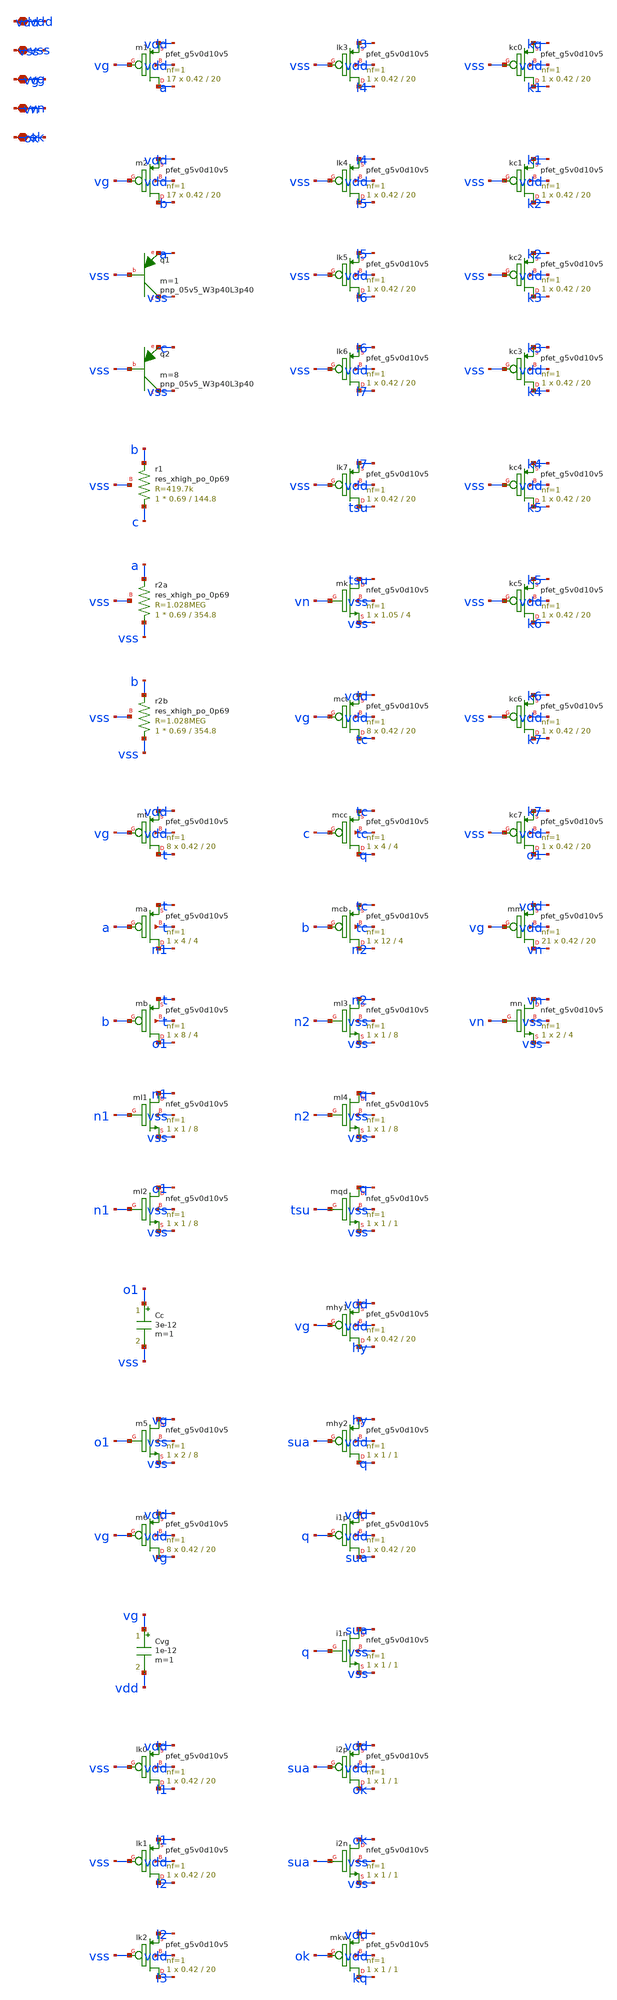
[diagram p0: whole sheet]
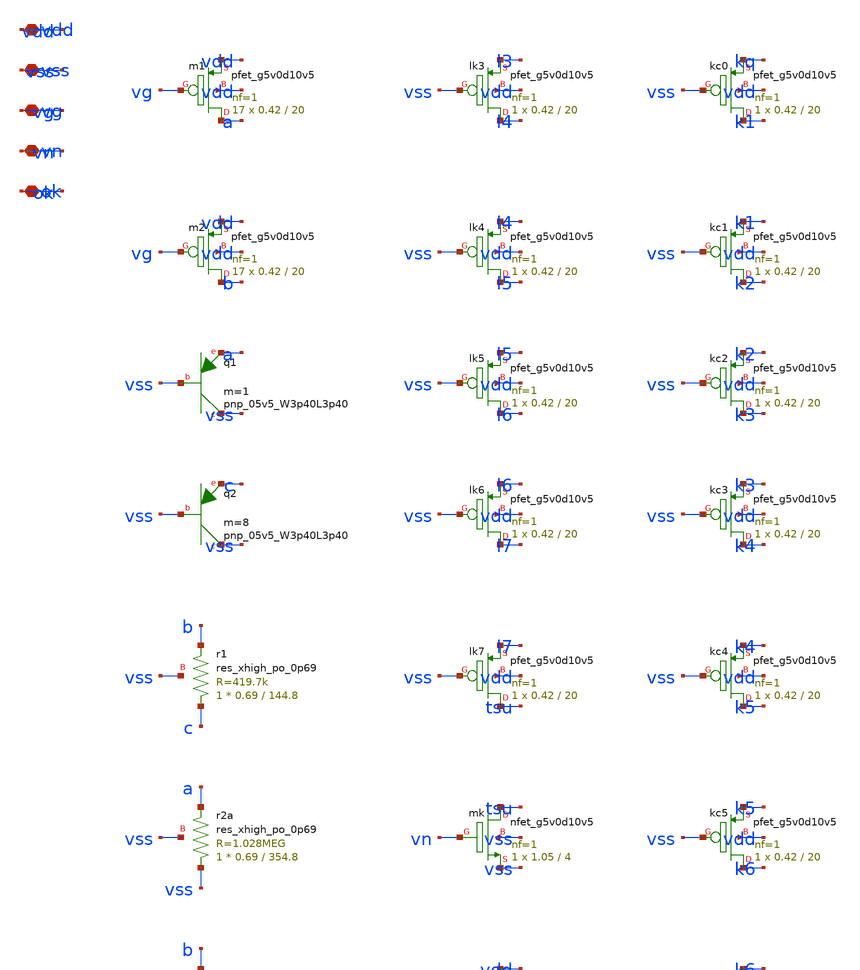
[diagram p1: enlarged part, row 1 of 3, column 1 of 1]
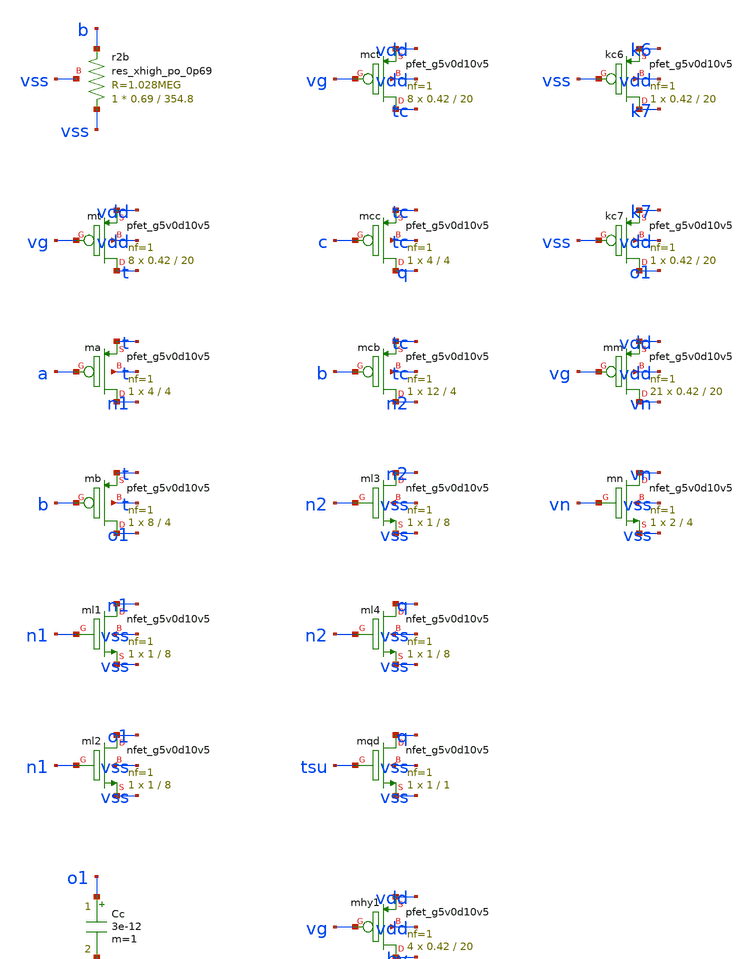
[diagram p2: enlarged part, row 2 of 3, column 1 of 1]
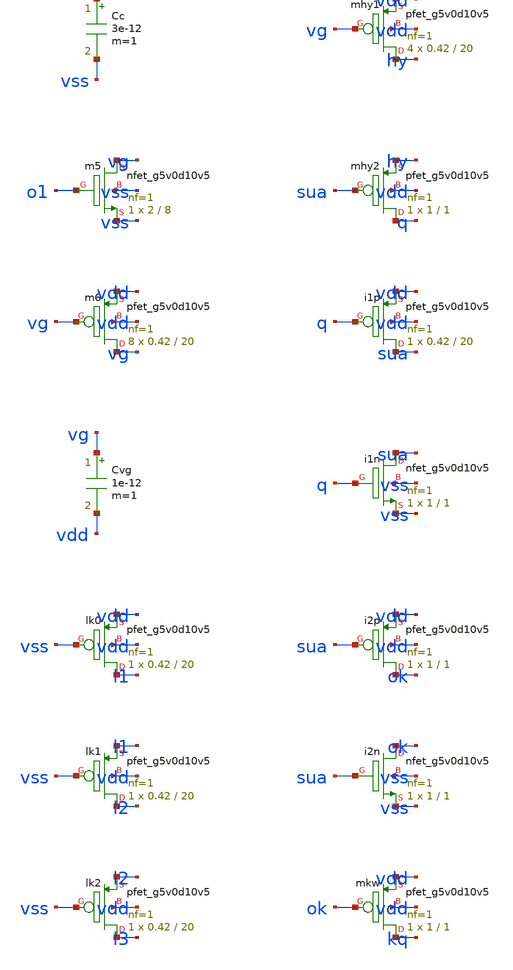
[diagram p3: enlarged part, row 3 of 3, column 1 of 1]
** sch_path: design/xschem/sch/c6_bias.sch
**.subckt c6_bias vdd vss vg vn ok
*.iopin vdd
*.iopin vss
*.iopin vg
*.iopin vn
*.iopin ok
Xm1 a vg vdd vdd sky130_fd_pr__pfet_g5v0d10v5 L=20 W=0.42 nf=1 ad='int((1 + 1)/2) * 0.42 / 1 * 0.29'
+ as='int((1 + 2)/2) * 0.42 / 1 * 0.29' pd='2*int((1 + 1)/2) * (0.42 / 1 + 0.29)' ps='2*int((1 + 2)/2) * (0.42 / 1 + 0.29)'
+ nrd='0.29 / 0.42 ' nrs='0.29 / 0.42 ' sa=0 sb=0 sd=0 mult=17 m=17
Xm2 b vg vdd vdd sky130_fd_pr__pfet_g5v0d10v5 L=20 W=0.42 nf=1 ad='int((1 + 1)/2) * 0.42 / 1 * 0.29'
+ as='int((1 + 2)/2) * 0.42 / 1 * 0.29' pd='2*int((1 + 1)/2) * (0.42 / 1 + 0.29)' ps='2*int((1 + 2)/2) * (0.42 / 1 + 0.29)'
+ nrd='0.29 / 0.42 ' nrs='0.29 / 0.42 ' sa=0 sb=0 sd=0 mult=17 m=17
Xq1 vss vss a sky130_fd_pr__pnp_05v5_W3p40L3p40 m=1
Xq2 vss vss c sky130_fd_pr__pnp_05v5_W3p40L3p40 m=8
Xr1 c b vss sky130_fd_pr__res_xhigh_po_0p69 L=144.8 mult=1 m=1
Xr2a vss a vss sky130_fd_pr__res_xhigh_po_0p69 L=354.8 mult=1 m=1
Xr2b vss b vss sky130_fd_pr__res_xhigh_po_0p69 L=354.8 mult=1 m=1
Xmt t vg vdd vdd sky130_fd_pr__pfet_g5v0d10v5 L=20 W=0.42 nf=1 ad='int((1 + 1)/2) * 0.42 / 1 * 0.29'
+ as='int((1 + 2)/2) * 0.42 / 1 * 0.29' pd='2*int((1 + 1)/2) * (0.42 / 1 + 0.29)' ps='2*int((1 + 2)/2) * (0.42 / 1 + 0.29)'
+ nrd='0.29 / 0.42 ' nrs='0.29 / 0.42 ' sa=0 sb=0 sd=0 mult=8 m=8
Xma n1 a t t sky130_fd_pr__pfet_g5v0d10v5 L=4 W=4 nf=1 ad='int((1 + 1)/2) * 4 / 1 * 0.29' as='int((1 + 2)/2) * 4 / 1 * 0.29'
+ pd='2*int((1 + 1)/2) * (4 / 1 + 0.29)' ps='2*int((1 + 2)/2) * (4 / 1 + 0.29)' nrd='0.29 / 4 ' nrs='0.29 / 4 '
+ sa=0 sb=0 sd=0 mult=1 m=1
Xmb o1 b t t sky130_fd_pr__pfet_g5v0d10v5 L=4 W=8 nf=1 ad='int((1 + 1)/2) * 8 / 1 * 0.29' as='int((1 + 2)/2) * 8 / 1 * 0.29'
+ pd='2*int((1 + 1)/2) * (8 / 1 + 0.29)' ps='2*int((1 + 2)/2) * (8 / 1 + 0.29)' nrd='0.29 / 8 ' nrs='0.29 / 8 '
+ sa=0 sb=0 sd=0 mult=1 m=1
Xml1 n1 n1 vss vss sky130_fd_pr__nfet_g5v0d10v5 L=8 W=1 nf=1 ad='int((1 + 1)/2) * 1 / 1 * 0.29' as='int((1 + 2)/2) * 1 / 1 * 0.29'
+ pd='2*int((1 + 1)/2) * (1 / 1 + 0.29)' ps='2*int((1 + 2)/2) * (1 / 1 + 0.29)' nrd='0.29 / 1 ' nrs='0.29 / 1 '
+ sa=0 sb=0 sd=0 mult=1 m=1
Xml2 o1 n1 vss vss sky130_fd_pr__nfet_g5v0d10v5 L=8 W=1 nf=1 ad='int((1 + 1)/2) * 1 / 1 * 0.29' as='int((1 + 2)/2) * 1 / 1 * 0.29'
+ pd='2*int((1 + 1)/2) * (1 / 1 + 0.29)' ps='2*int((1 + 2)/2) * (1 / 1 + 0.29)' nrd='0.29 / 1 ' nrs='0.29 / 1 '
+ sa=0 sb=0 sd=0 mult=1 m=1
Cc o1 vss 3e-12 m=1
Xm5 vg o1 vss vss sky130_fd_pr__nfet_g5v0d10v5 L=8 W=2 nf=1 ad='int((1 + 1)/2) * 2 / 1 * 0.29' as='int((1 + 2)/2) * 2 / 1 * 0.29'
+ pd='2*int((1 + 1)/2) * (2 / 1 + 0.29)' ps='2*int((1 + 2)/2) * (2 / 1 + 0.29)' nrd='0.29 / 2 ' nrs='0.29 / 2 '
+ sa=0 sb=0 sd=0 mult=1 m=1
Xm6 vg vg vdd vdd sky130_fd_pr__pfet_g5v0d10v5 L=20 W=0.42 nf=1 ad='int((1 + 1)/2) * 0.42 / 1 * 0.29'
+ as='int((1 + 2)/2) * 0.42 / 1 * 0.29' pd='2*int((1 + 1)/2) * (0.42 / 1 + 0.29)' ps='2*int((1 + 2)/2) * (0.42 / 1 + 0.29)'
+ nrd='0.29 / 0.42 ' nrs='0.29 / 0.42 ' sa=0 sb=0 sd=0 mult=8 m=8
Cvg vg vdd 1e-12 m=1
Xlk0 l1 vss vdd vdd sky130_fd_pr__pfet_g5v0d10v5 L=20 W=0.42 nf=1 ad='int((1 + 1)/2) * 0.42 / 1 * 0.29'
+ as='int((1 + 2)/2) * 0.42 / 1 * 0.29' pd='2*int((1 + 1)/2) * (0.42 / 1 + 0.29)' ps='2*int((1 + 2)/2) * (0.42 / 1 + 0.29)'
+ nrd='0.29 / 0.42 ' nrs='0.29 / 0.42 ' sa=0 sb=0 sd=0 mult=1 m=1
Xlk1 l2 vss l1 vdd sky130_fd_pr__pfet_g5v0d10v5 L=20 W=0.42 nf=1 ad='int((1 + 1)/2) * 0.42 / 1 * 0.29'
+ as='int((1 + 2)/2) * 0.42 / 1 * 0.29' pd='2*int((1 + 1)/2) * (0.42 / 1 + 0.29)' ps='2*int((1 + 2)/2) * (0.42 / 1 + 0.29)'
+ nrd='0.29 / 0.42 ' nrs='0.29 / 0.42 ' sa=0 sb=0 sd=0 mult=1 m=1
Xlk2 l3 vss l2 vdd sky130_fd_pr__pfet_g5v0d10v5 L=20 W=0.42 nf=1 ad='int((1 + 1)/2) * 0.42 / 1 * 0.29'
+ as='int((1 + 2)/2) * 0.42 / 1 * 0.29' pd='2*int((1 + 1)/2) * (0.42 / 1 + 0.29)' ps='2*int((1 + 2)/2) * (0.42 / 1 + 0.29)'
+ nrd='0.29 / 0.42 ' nrs='0.29 / 0.42 ' sa=0 sb=0 sd=0 mult=1 m=1
Xlk3 l4 vss l3 vdd sky130_fd_pr__pfet_g5v0d10v5 L=20 W=0.42 nf=1 ad='int((1 + 1)/2) * 0.42 / 1 * 0.29'
+ as='int((1 + 2)/2) * 0.42 / 1 * 0.29' pd='2*int((1 + 1)/2) * (0.42 / 1 + 0.29)' ps='2*int((1 + 2)/2) * (0.42 / 1 + 0.29)'
+ nrd='0.29 / 0.42 ' nrs='0.29 / 0.42 ' sa=0 sb=0 sd=0 mult=1 m=1
Xlk4 l5 vss l4 vdd sky130_fd_pr__pfet_g5v0d10v5 L=20 W=0.42 nf=1 ad='int((1 + 1)/2) * 0.42 / 1 * 0.29'
+ as='int((1 + 2)/2) * 0.42 / 1 * 0.29' pd='2*int((1 + 1)/2) * (0.42 / 1 + 0.29)' ps='2*int((1 + 2)/2) * (0.42 / 1 + 0.29)'
+ nrd='0.29 / 0.42 ' nrs='0.29 / 0.42 ' sa=0 sb=0 sd=0 mult=1 m=1
Xlk5 l6 vss l5 vdd sky130_fd_pr__pfet_g5v0d10v5 L=20 W=0.42 nf=1 ad='int((1 + 1)/2) * 0.42 / 1 * 0.29'
+ as='int((1 + 2)/2) * 0.42 / 1 * 0.29' pd='2*int((1 + 1)/2) * (0.42 / 1 + 0.29)' ps='2*int((1 + 2)/2) * (0.42 / 1 + 0.29)'
+ nrd='0.29 / 0.42 ' nrs='0.29 / 0.42 ' sa=0 sb=0 sd=0 mult=1 m=1
Xlk6 l7 vss l6 vdd sky130_fd_pr__pfet_g5v0d10v5 L=20 W=0.42 nf=1 ad='int((1 + 1)/2) * 0.42 / 1 * 0.29'
+ as='int((1 + 2)/2) * 0.42 / 1 * 0.29' pd='2*int((1 + 1)/2) * (0.42 / 1 + 0.29)' ps='2*int((1 + 2)/2) * (0.42 / 1 + 0.29)'
+ nrd='0.29 / 0.42 ' nrs='0.29 / 0.42 ' sa=0 sb=0 sd=0 mult=1 m=1
Xlk7 tsu vss l7 vdd sky130_fd_pr__pfet_g5v0d10v5 L=20 W=0.42 nf=1 ad='int((1 + 1)/2) * 0.42 / 1 * 0.29'
+ as='int((1 + 2)/2) * 0.42 / 1 * 0.29' pd='2*int((1 + 1)/2) * (0.42 / 1 + 0.29)' ps='2*int((1 + 2)/2) * (0.42 / 1 + 0.29)'
+ nrd='0.29 / 0.42 ' nrs='0.29 / 0.42 ' sa=0 sb=0 sd=0 mult=1 m=1
Xmk tsu vn vss vss sky130_fd_pr__nfet_g5v0d10v5 L=4 W=1.05 nf=1 ad='int((1 + 1)/2) * 1.05 / 1 * 0.29'
+ as='int((1 + 2)/2) * 1.05 / 1 * 0.29' pd='2*int((1 + 1)/2) * (1.05 / 1 + 0.29)' ps='2*int((1 + 2)/2) * (1.05 / 1 + 0.29)'
+ nrd='0.29 / 1.05 ' nrs='0.29 / 1.05 ' sa=0 sb=0 sd=0 mult=1 m=1
Xmct tc vg vdd vdd sky130_fd_pr__pfet_g5v0d10v5 L=20 W=0.42 nf=1 ad='int((1 + 1)/2) * 0.42 / 1 * 0.29'
+ as='int((1 + 2)/2) * 0.42 / 1 * 0.29' pd='2*int((1 + 1)/2) * (0.42 / 1 + 0.29)' ps='2*int((1 + 2)/2) * (0.42 / 1 + 0.29)'
+ nrd='0.29 / 0.42 ' nrs='0.29 / 0.42 ' sa=0 sb=0 sd=0 mult=8 m=8
Xmcc q c tc tc sky130_fd_pr__pfet_g5v0d10v5 L=4 W=4 nf=1 ad='int((1 + 1)/2) * 4 / 1 * 0.29' as='int((1 + 2)/2) * 4 / 1 * 0.29'
+ pd='2*int((1 + 1)/2) * (4 / 1 + 0.29)' ps='2*int((1 + 2)/2) * (4 / 1 + 0.29)' nrd='0.29 / 4 ' nrs='0.29 / 4 '
+ sa=0 sb=0 sd=0 mult=1 m=1
Xmcb n2 b tc tc sky130_fd_pr__pfet_g5v0d10v5 L=4 W=12 nf=1 ad='int((1 + 1)/2) * 12 / 1 * 0.29' as='int((1 + 2)/2) * 12 / 1 * 0.29'
+ pd='2*int((1 + 1)/2) * (12 / 1 + 0.29)' ps='2*int((1 + 2)/2) * (12 / 1 + 0.29)' nrd='0.29 / 12 ' nrs='0.29 / 12 '
+ sa=0 sb=0 sd=0 mult=1 m=1
Xml3 n2 n2 vss vss sky130_fd_pr__nfet_g5v0d10v5 L=8 W=1 nf=1 ad='int((1 + 1)/2) * 1 / 1 * 0.29' as='int((1 + 2)/2) * 1 / 1 * 0.29'
+ pd='2*int((1 + 1)/2) * (1 / 1 + 0.29)' ps='2*int((1 + 2)/2) * (1 / 1 + 0.29)' nrd='0.29 / 1 ' nrs='0.29 / 1 '
+ sa=0 sb=0 sd=0 mult=1 m=1
Xml4 q n2 vss vss sky130_fd_pr__nfet_g5v0d10v5 L=8 W=1 nf=1 ad='int((1 + 1)/2) * 1 / 1 * 0.29' as='int((1 + 2)/2) * 1 / 1 * 0.29'
+ pd='2*int((1 + 1)/2) * (1 / 1 + 0.29)' ps='2*int((1 + 2)/2) * (1 / 1 + 0.29)' nrd='0.29 / 1 ' nrs='0.29 / 1 '
+ sa=0 sb=0 sd=0 mult=1 m=1
Xmqd q tsu vss vss sky130_fd_pr__nfet_g5v0d10v5 L=1 W=1 nf=1 ad='int((1 + 1)/2) * 1 / 1 * 0.29' as='int((1 + 2)/2) * 1 / 1 * 0.29'
+ pd='2*int((1 + 1)/2) * (1 / 1 + 0.29)' ps='2*int((1 + 2)/2) * (1 / 1 + 0.29)' nrd='0.29 / 1 ' nrs='0.29 / 1 '
+ sa=0 sb=0 sd=0 mult=1 m=1
Xmhy1 hy vg vdd vdd sky130_fd_pr__pfet_g5v0d10v5 L=20 W=0.42 nf=1 ad='int((1 + 1)/2) * 0.42 / 1 * 0.29'
+ as='int((1 + 2)/2) * 0.42 / 1 * 0.29' pd='2*int((1 + 1)/2) * (0.42 / 1 + 0.29)' ps='2*int((1 + 2)/2) * (0.42 / 1 + 0.29)'
+ nrd='0.29 / 0.42 ' nrs='0.29 / 0.42 ' sa=0 sb=0 sd=0 mult=4 m=4
Xmhy2 q sua hy vdd sky130_fd_pr__pfet_g5v0d10v5 L=1 W=1 nf=1 ad='int((1 + 1)/2) * 1 / 1 * 0.29' as='int((1 + 2)/2) * 1 / 1 * 0.29'
+ pd='2*int((1 + 1)/2) * (1 / 1 + 0.29)' ps='2*int((1 + 2)/2) * (1 / 1 + 0.29)' nrd='0.29 / 1 ' nrs='0.29 / 1 '
+ sa=0 sb=0 sd=0 mult=1 m=1
Xi1p sua q vdd vdd sky130_fd_pr__pfet_g5v0d10v5 L=20 W=0.42 nf=1 ad='int((1 + 1)/2) * 0.42 / 1 * 0.29'
+ as='int((1 + 2)/2) * 0.42 / 1 * 0.29' pd='2*int((1 + 1)/2) * (0.42 / 1 + 0.29)' ps='2*int((1 + 2)/2) * (0.42 / 1 + 0.29)'
+ nrd='0.29 / 0.42 ' nrs='0.29 / 0.42 ' sa=0 sb=0 sd=0 mult=1 m=1
Xi1n sua q vss vss sky130_fd_pr__nfet_g5v0d10v5 L=1 W=1 nf=1 ad='int((1 + 1)/2) * 1 / 1 * 0.29' as='int((1 + 2)/2) * 1 / 1 * 0.29'
+ pd='2*int((1 + 1)/2) * (1 / 1 + 0.29)' ps='2*int((1 + 2)/2) * (1 / 1 + 0.29)' nrd='0.29 / 1 ' nrs='0.29 / 1 '
+ sa=0 sb=0 sd=0 mult=1 m=1
Xi2p ok sua vdd vdd sky130_fd_pr__pfet_g5v0d10v5 L=1 W=1 nf=1 ad='int((1 + 1)/2) * 1 / 1 * 0.29' as='int((1 + 2)/2) * 1 / 1 * 0.29'
+ pd='2*int((1 + 1)/2) * (1 / 1 + 0.29)' ps='2*int((1 + 2)/2) * (1 / 1 + 0.29)' nrd='0.29 / 1 ' nrs='0.29 / 1 '
+ sa=0 sb=0 sd=0 mult=1 m=1
Xi2n ok sua vss vss sky130_fd_pr__nfet_g5v0d10v5 L=1 W=1 nf=1 ad='int((1 + 1)/2) * 1 / 1 * 0.29' as='int((1 + 2)/2) * 1 / 1 * 0.29'
+ pd='2*int((1 + 1)/2) * (1 / 1 + 0.29)' ps='2*int((1 + 2)/2) * (1 / 1 + 0.29)' nrd='0.29 / 1 ' nrs='0.29 / 1 '
+ sa=0 sb=0 sd=0 mult=1 m=1
Xmkw kq ok vdd vdd sky130_fd_pr__pfet_g5v0d10v5 L=1 W=1 nf=1 ad='int((1 + 1)/2) * 1 / 1 * 0.29' as='int((1 + 2)/2) * 1 / 1 * 0.29'
+ pd='2*int((1 + 1)/2) * (1 / 1 + 0.29)' ps='2*int((1 + 2)/2) * (1 / 1 + 0.29)' nrd='0.29 / 1 ' nrs='0.29 / 1 '
+ sa=0 sb=0 sd=0 mult=1 m=1
Xkc0 k1 vss kq vdd sky130_fd_pr__pfet_g5v0d10v5 L=20 W=0.42 nf=1 ad='int((1 + 1)/2) * 0.42 / 1 * 0.29'
+ as='int((1 + 2)/2) * 0.42 / 1 * 0.29' pd='2*int((1 + 1)/2) * (0.42 / 1 + 0.29)' ps='2*int((1 + 2)/2) * (0.42 / 1 + 0.29)'
+ nrd='0.29 / 0.42 ' nrs='0.29 / 0.42 ' sa=0 sb=0 sd=0 mult=1 m=1
Xkc1 k2 vss k1 vdd sky130_fd_pr__pfet_g5v0d10v5 L=20 W=0.42 nf=1 ad='int((1 + 1)/2) * 0.42 / 1 * 0.29'
+ as='int((1 + 2)/2) * 0.42 / 1 * 0.29' pd='2*int((1 + 1)/2) * (0.42 / 1 + 0.29)' ps='2*int((1 + 2)/2) * (0.42 / 1 + 0.29)'
+ nrd='0.29 / 0.42 ' nrs='0.29 / 0.42 ' sa=0 sb=0 sd=0 mult=1 m=1
Xkc2 k3 vss k2 vdd sky130_fd_pr__pfet_g5v0d10v5 L=20 W=0.42 nf=1 ad='int((1 + 1)/2) * 0.42 / 1 * 0.29'
+ as='int((1 + 2)/2) * 0.42 / 1 * 0.29' pd='2*int((1 + 1)/2) * (0.42 / 1 + 0.29)' ps='2*int((1 + 2)/2) * (0.42 / 1 + 0.29)'
+ nrd='0.29 / 0.42 ' nrs='0.29 / 0.42 ' sa=0 sb=0 sd=0 mult=1 m=1
Xkc3 k4 vss k3 vdd sky130_fd_pr__pfet_g5v0d10v5 L=20 W=0.42 nf=1 ad='int((1 + 1)/2) * 0.42 / 1 * 0.29'
+ as='int((1 + 2)/2) * 0.42 / 1 * 0.29' pd='2*int((1 + 1)/2) * (0.42 / 1 + 0.29)' ps='2*int((1 + 2)/2) * (0.42 / 1 + 0.29)'
+ nrd='0.29 / 0.42 ' nrs='0.29 / 0.42 ' sa=0 sb=0 sd=0 mult=1 m=1
Xkc4 k5 vss k4 vdd sky130_fd_pr__pfet_g5v0d10v5 L=20 W=0.42 nf=1 ad='int((1 + 1)/2) * 0.42 / 1 * 0.29'
+ as='int((1 + 2)/2) * 0.42 / 1 * 0.29' pd='2*int((1 + 1)/2) * (0.42 / 1 + 0.29)' ps='2*int((1 + 2)/2) * (0.42 / 1 + 0.29)'
+ nrd='0.29 / 0.42 ' nrs='0.29 / 0.42 ' sa=0 sb=0 sd=0 mult=1 m=1
Xkc5 k6 vss k5 vdd sky130_fd_pr__pfet_g5v0d10v5 L=20 W=0.42 nf=1 ad='int((1 + 1)/2) * 0.42 / 1 * 0.29'
+ as='int((1 + 2)/2) * 0.42 / 1 * 0.29' pd='2*int((1 + 1)/2) * (0.42 / 1 + 0.29)' ps='2*int((1 + 2)/2) * (0.42 / 1 + 0.29)'
+ nrd='0.29 / 0.42 ' nrs='0.29 / 0.42 ' sa=0 sb=0 sd=0 mult=1 m=1
Xkc6 k7 vss k6 vdd sky130_fd_pr__pfet_g5v0d10v5 L=20 W=0.42 nf=1 ad='int((1 + 1)/2) * 0.42 / 1 * 0.29'
+ as='int((1 + 2)/2) * 0.42 / 1 * 0.29' pd='2*int((1 + 1)/2) * (0.42 / 1 + 0.29)' ps='2*int((1 + 2)/2) * (0.42 / 1 + 0.29)'
+ nrd='0.29 / 0.42 ' nrs='0.29 / 0.42 ' sa=0 sb=0 sd=0 mult=1 m=1
Xkc7 o1 vss k7 vdd sky130_fd_pr__pfet_g5v0d10v5 L=20 W=0.42 nf=1 ad='int((1 + 1)/2) * 0.42 / 1 * 0.29'
+ as='int((1 + 2)/2) * 0.42 / 1 * 0.29' pd='2*int((1 + 1)/2) * (0.42 / 1 + 0.29)' ps='2*int((1 + 2)/2) * (0.42 / 1 + 0.29)'
+ nrd='0.29 / 0.42 ' nrs='0.29 / 0.42 ' sa=0 sb=0 sd=0 mult=1 m=1
Xmm vn vg vdd vdd sky130_fd_pr__pfet_g5v0d10v5 L=20 W=0.42 nf=1 ad='int((1 + 1)/2) * 0.42 / 1 * 0.29'
+ as='int((1 + 2)/2) * 0.42 / 1 * 0.29' pd='2*int((1 + 1)/2) * (0.42 / 1 + 0.29)' ps='2*int((1 + 2)/2) * (0.42 / 1 + 0.29)'
+ nrd='0.29 / 0.42 ' nrs='0.29 / 0.42 ' sa=0 sb=0 sd=0 mult=21 m=21
Xmn vn vn vss vss sky130_fd_pr__nfet_g5v0d10v5 L=4 W=2 nf=1 ad='int((1 + 1)/2) * 2 / 1 * 0.29' as='int((1 + 2)/2) * 2 / 1 * 0.29'
+ pd='2*int((1 + 1)/2) * (2 / 1 + 0.29)' ps='2*int((1 + 2)/2) * (2 / 1 + 0.29)' nrd='0.29 / 2 ' nrs='0.29 / 2 '
+ sa=0 sb=0 sd=0 mult=1 m=1
**.ends
.end
